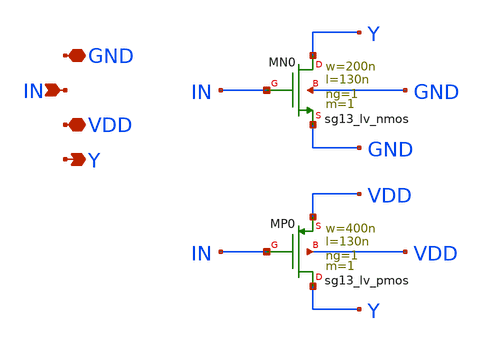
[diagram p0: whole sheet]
** sch_path: SoC6169-main/schematic/xschem/INV.sch
* Copyright 2026 USFQ CAM team
* Licensed under the Apache License, Version 2.0 (the "License");
* you may not use this file except in compliance with the License.
* You may obtain a copy of the License at
* https://www.apache.org/licenses/LICENSE-2.0
* Unless required by applicable law or agreed to in writing, software
* distributed under the License is distributed on an "AS IS" BASIS,
* WITHOUT WARRANTIES OR CONDITIONS OF ANY KIND, either express or implied.
* See the License for the specific language governing permissions and
* limitations under the License.
**.subckt INV GND IN VDD Y
*.iopin GND
*.ipin IN
*.iopin VDD
*.opin Y
XMN0 Y IN GND GND sg13_lv_nmos w=200n l=130n ng=1 m=1 mm_ok=1
XMP0 Y IN VDD VDD sg13_lv_pmos w=400n l=130n ng=1 m=1 mm_ok=1
**.ends
.end
